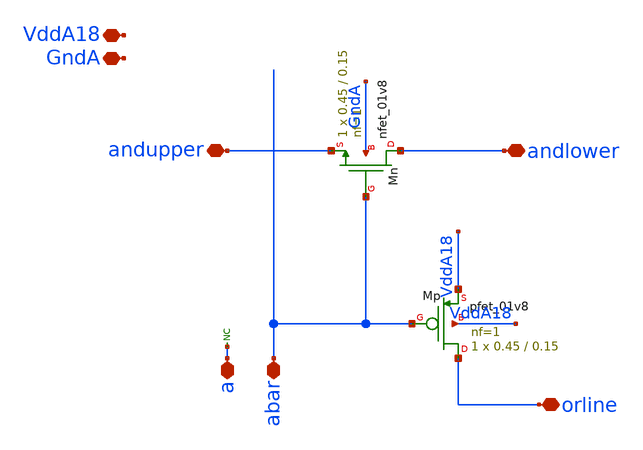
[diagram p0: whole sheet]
** sch_path: analog/xschem/BiasDecCB0.sch
**.subckt BiasDecCB0 GndA VddA18 orline andlower andupper abar a
*.iopin GndA
*.iopin VddA18
*.iopin orline
*.iopin andlower
*.iopin andupper
*.iopin abar
*.iopin a
XMp orline abar VddA18 VddA18 sky130_fd_pr__pfet_01v8 L=0.15 W=0.45 nf=1 ad='int((1 + 1)/2) * 0.45 / 1 * 0.29'
+ as='int((1 + 2)/2) * 0.45 / 1 * 0.29' pd='2*int((1 + 1)/2) * (0.45 / 1 + 0.29)' ps='2*int((1 + 2)/2) * (0.45 / 1 + 0.29)'
+ nrd='0.29 / 0.45 ' nrs='0.29 / 0.45 ' sa=0 sb=0 sd=0 mult=1 m=1
XMn andlower abar andupper GndA sky130_fd_pr__nfet_01v8 L=0.15 W=0.45 nf=1 ad='int((1 + 1)/2) * 0.45 / 1 * 0.29'
+ as='int((1 + 2)/2) * 0.45 / 1 * 0.29' pd='2*int((1 + 1)/2) * (0.45 / 1 + 0.29)' ps='2*int((1 + 2)/2) * (0.45 / 1 + 0.29)'
+ nrd='0.29 / 0.45 ' nrs='0.29 / 0.45 ' sa=0 sb=0 sd=0 mult=1 m=1
* noconn a
**.ends
.end
